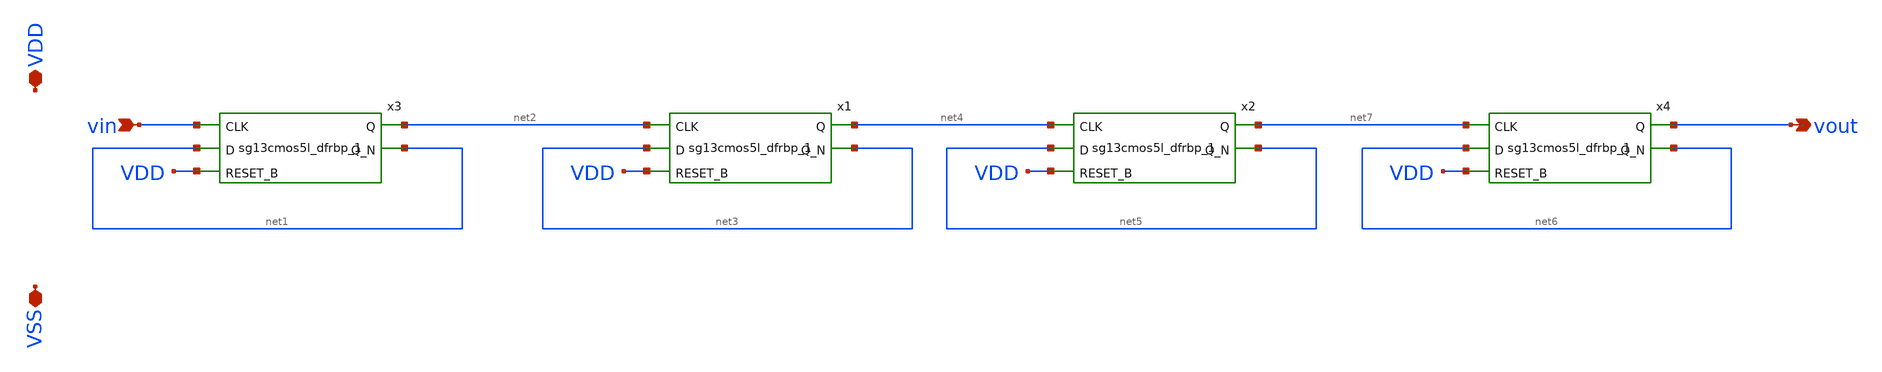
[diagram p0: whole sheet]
** sch_path: macros/heichips26_ook/macros/ook_analog_system/schematic/xschem/clock_divider.sch
**.subckt clock_divider vin VDD VSS vout
*.ipin vin
*.iopin VDD
*.iopin VSS
*.opin vout
x3 net2 net1 vin net1 VDD VDD VSS sg13cmos5l_dfrbp_1
x1 net4 net3 net2 net3 VDD VDD VSS sg13cmos5l_dfrbp_1
x2 net7 net5 net4 net5 VDD VDD VSS sg13cmos5l_dfrbp_1
x4 vout net6 net7 net6 VDD VDD VSS sg13cmos5l_dfrbp_1
**.ends
.end
